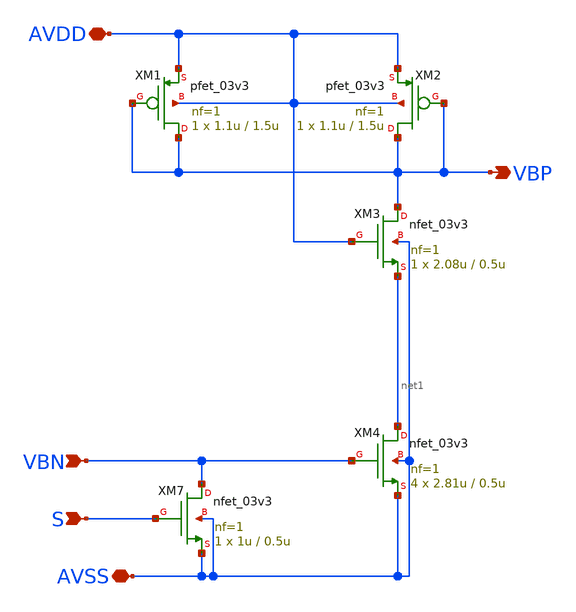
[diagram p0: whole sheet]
** sch_path: designs/libs/core_analog/feed_forward_zero/feed_forward_zero_v2.sch
**.subckt feed_forward_zero_v2 VBP AVDD AVSS VBN S
*.opin VBP
*.iopin AVDD
*.iopin AVSS
*.ipin VBN
*.ipin S
XM1 VBP VBP AVDD AVDD pfet_03v3 L=1.5u W=1.1u nf=1 ad='int((nf+1)/2) * W/nf * 0.18u' as='int((nf+2)/2) * W/nf * 0.18u'
+ pd='2*int((nf+1)/2) * (W/nf + 0.18u)' ps='2*int((nf+2)/2) * (W/nf + 0.18u)' nrd='0.18u / W' nrs='0.18u / W'
+ sa=0 sb=0 sd=0 m=1
XM3 VBP AVDD net1 AVSS nfet_03v3 L=0.5u W=2.08u nf=1 ad='int((nf+1)/2) * W/nf * 0.18u' as='int((nf+2)/2) * W/nf * 0.18u'
+ pd='2*int((nf+1)/2) * (W/nf + 0.18u)' ps='2*int((nf+2)/2) * (W/nf + 0.18u)' nrd='0.18u / W' nrs='0.18u / W'
+ sa=0 sb=0 sd=0 m=1
XM4 net1 VBN AVSS AVSS nfet_03v3 L=0.5u W=2.81u nf=1 ad='int((nf+1)/2) * W/nf * 0.18u' as='int((nf+2)/2) * W/nf * 0.18u'
+ pd='2*int((nf+1)/2) * (W/nf + 0.18u)' ps='2*int((nf+2)/2) * (W/nf + 0.18u)' nrd='0.18u / W' nrs='0.18u / W'
+ sa=0 sb=0 sd=0 m=4
XM7 VBN S AVSS AVSS nfet_03v3 L=0.5u W=1u nf=1 ad='int((nf+1)/2) * W/nf * 0.18u' as='int((nf+2)/2) * W/nf * 0.18u'
+ pd='2*int((nf+1)/2) * (W/nf + 0.18u)' ps='2*int((nf+2)/2) * (W/nf + 0.18u)' nrd='0.18u / W' nrs='0.18u / W'
+ sa=0 sb=0 sd=0 m=1
XM2 VBP VBP AVDD AVDD pfet_03v3 L=1.5u W=1.1u nf=1 ad='int((nf+1)/2) * W/nf * 0.18u' as='int((nf+2)/2) * W/nf * 0.18u'
+ pd='2*int((nf+1)/2) * (W/nf + 0.18u)' ps='2*int((nf+2)/2) * (W/nf + 0.18u)' nrd='0.18u / W' nrs='0.18u / W'
+ sa=0 sb=0 sd=0 m=1
**.ends
.end
